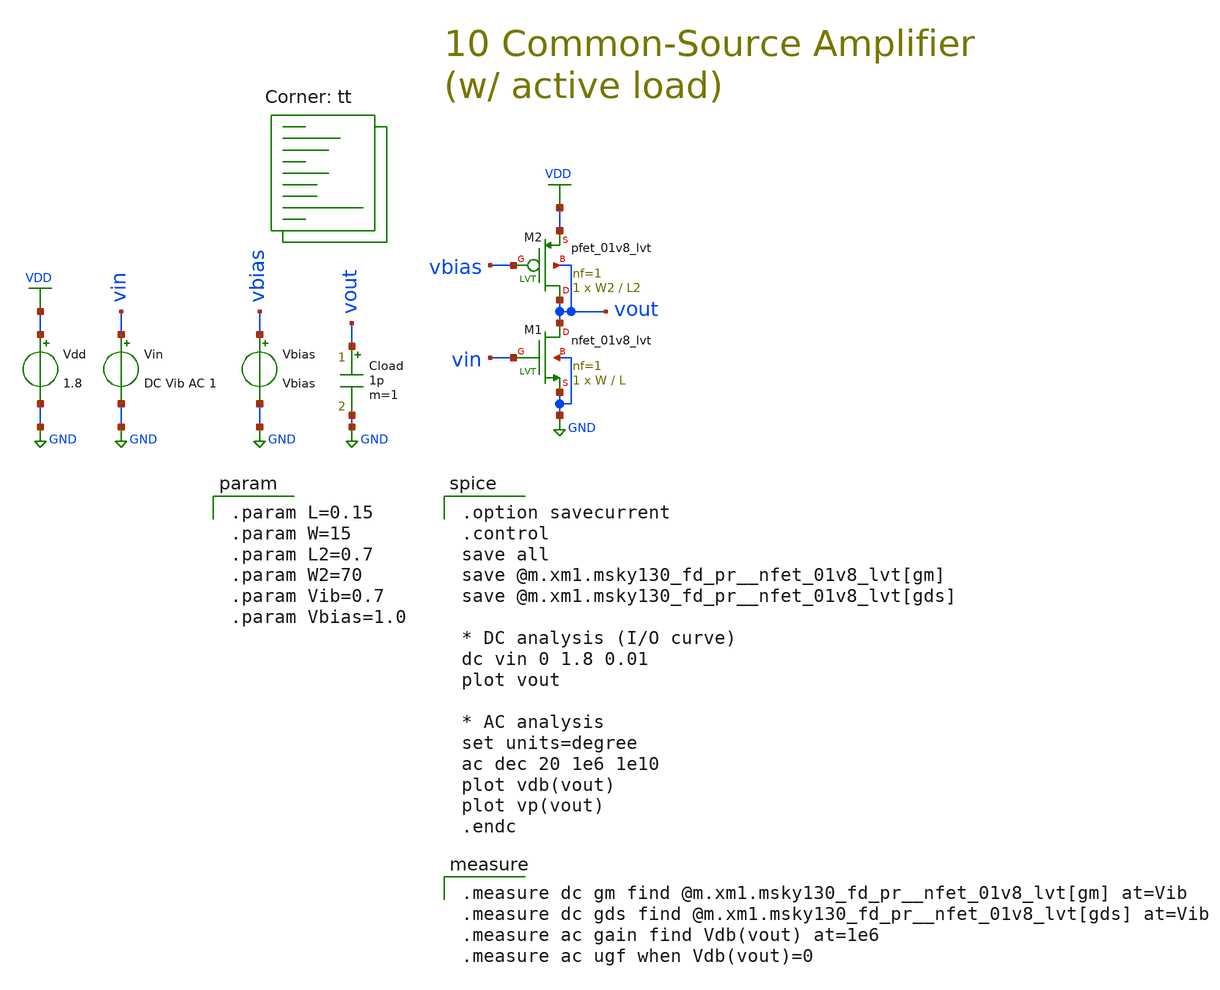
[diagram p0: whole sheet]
** sch_path: 10-a_common-source-amp.sch
**.subckt 10-a_common-source-amp
XM1 vout vin GND GND sky130_fd_pr__nfet_01v8_lvt L=L W=W nf=1 ad='int((1 + 1)/2) * W / 1 * 0.29' as='int((1 + 2)/2) * W / 1 * 0.29'
+ pd='2*int((1 + 1)/2) * (W / 1 + 0.29)' ps='2*int((1 + 2)/2) * (W / 1 + 0.29)' nrd='0.29 / W ' nrs='0.29 / W '
+ sa=0 sb=0 sd=0 mult=1 m=1
Vdd VDD GND 1.8
Vin vin GND DC Vib AC 1
Cload vout GND 1p m=1
Vbias vbias GND Vbias
XM2 vout vbias VDD vout sky130_fd_pr__pfet_01v8_lvt L=L2 W=W2 nf=1 ad='int((1 + 1)/2) * W2 / 1 * 0.29'
+ as='int((1 + 2)/2) * W2 / 1 * 0.29' pd='2*int((1 + 1)/2) * (W2 / 1 + 0.29)' ps='2*int((1 + 2)/2) * (W2 / 1 + 0.29)'
+ nrd='0.29 / W2 ' nrs='0.29 / W2 ' sa=0 sb=0 sd=0 mult=1 m=1
**** begin user architecture code
.lib $::SKYWATER_MODELS/sky130.lib.spice tt

.param L=0.15
.param W=15
.param L2=0.7
.param W2=70
.param Vib=0.7
.param Vbias=1.0


.option savecurrent
.control
save all
save @m.xm1.msky130_fd_pr__nfet_01v8_lvt[gm]
save @m.xm1.msky130_fd_pr__nfet_01v8_lvt[gds]

* DC analysis (I/O curve)
dc vin 0 1.8 0.01
plot vout

* AC analysis
set units=degree
ac dec 20 1e6 1e10
plot vdb(vout)
plot vp(vout)
.endc


.measure dc gm find @m.xm1.msky130_fd_pr__nfet_01v8_lvt[gm] at=Vib
.measure dc gds find @m.xm1.msky130_fd_pr__nfet_01v8_lvt[gds] at=Vib
.measure ac gain find Vdb(vout) at=1e6
.measure ac ugf when Vdb(vout)=0

**** end user architecture code
**.ends
.GLOBAL GND
.GLOBAL VDD
.end
